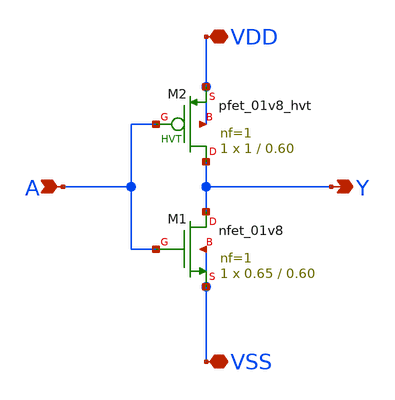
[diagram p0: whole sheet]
** sch_path: custom_gds/tt_um_mickey_pll/xschem/inv_0p25.sch
**.subckt inv_0p25 A VDD VSS Y
*.ipin A
*.iopin VDD
*.iopin VSS
*.opin Y
XM1 Y A VSS VSS sky130_fd_pr__nfet_01v8 L=0.60 W=0.65 nf=1 ad='int((nf+1)/2) * W/nf * 0.29' as='int((nf+2)/2) * W/nf * 0.29'
+ pd='2*int((nf+1)/2) * (W/nf + 0.29)' ps='2*int((nf+2)/2) * (W/nf + 0.29)' nrd='0.29 / W' nrs='0.29 / W'
+ sa=0 sb=0 sd=0 mult=1 m=1
XM2 Y A VDD VDD sky130_fd_pr__pfet_01v8_hvt L=0.60 W=1 nf=1 ad='int((nf+1)/2) * W/nf * 0.29' as='int((nf+2)/2) * W/nf * 0.29'
+ pd='2*int((nf+1)/2) * (W/nf + 0.29)' ps='2*int((nf+2)/2) * (W/nf + 0.29)' nrd='0.29 / W' nrs='0.29 / W'
+ sa=0 sb=0 sd=0 mult=1 m=1
**.ends
.end
